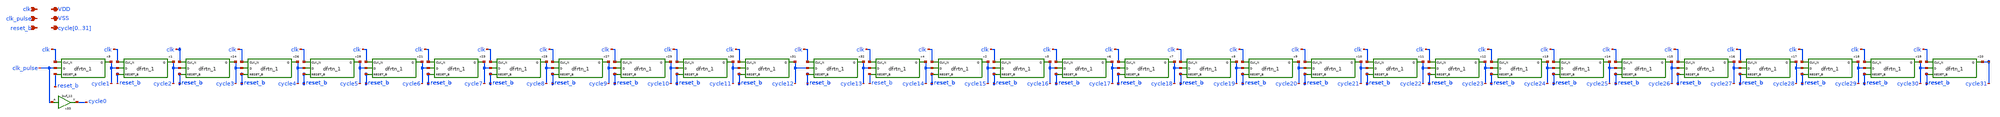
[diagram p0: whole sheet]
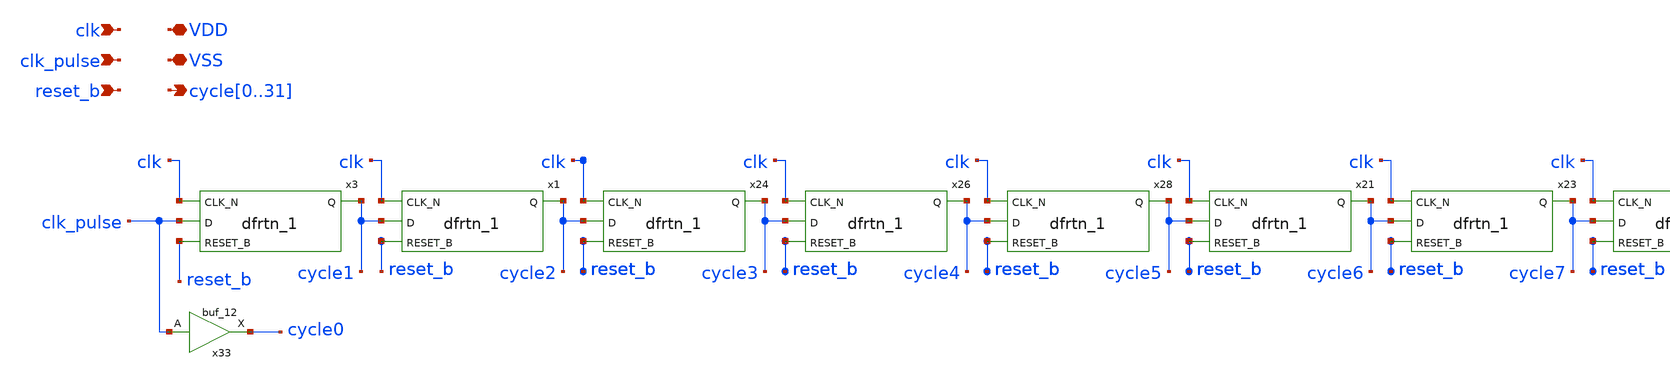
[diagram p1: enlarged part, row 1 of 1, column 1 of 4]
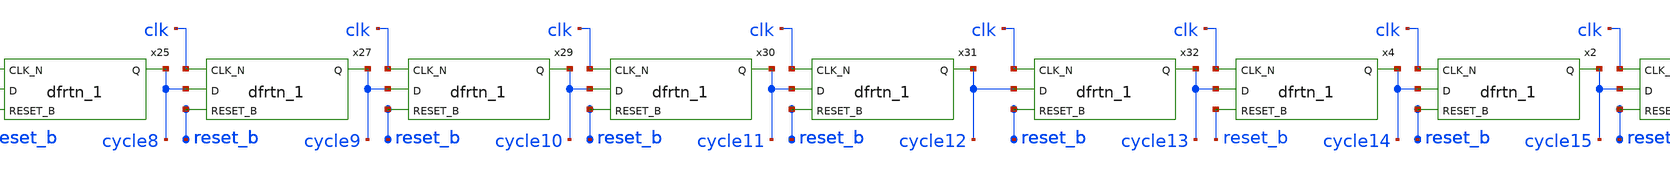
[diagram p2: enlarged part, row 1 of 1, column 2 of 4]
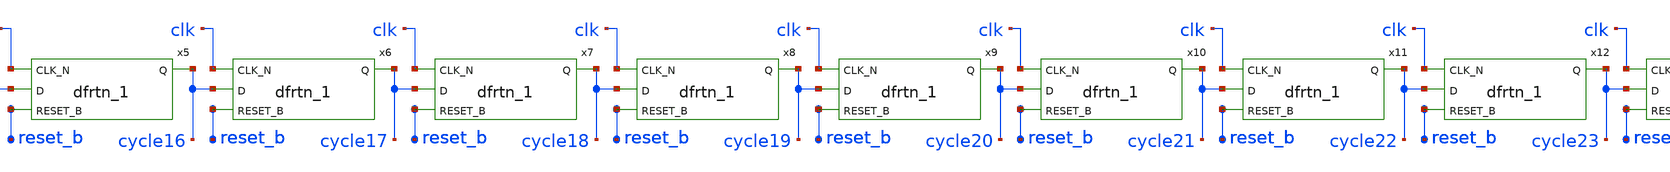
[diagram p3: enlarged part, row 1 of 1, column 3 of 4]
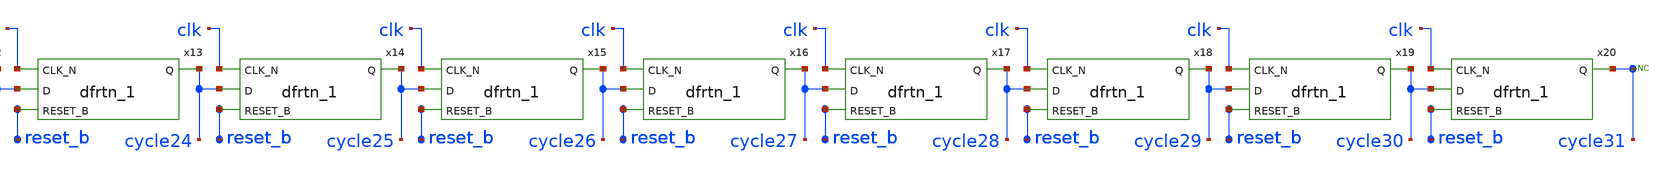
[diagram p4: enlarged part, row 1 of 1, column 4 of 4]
** sch_path: xschem/src/clock_pulse_delay_line/clock_pulse_delay_line.sch
**.subckt clock_pulse_delay_line clk_pulse
*+ cycle0,cycle1,cycle2,cycle3,cycle4,cycle5,cycle6,cycle7,cycle8,cycle9,cycle10,cycle11,cycle12,cycle13,cycle14,cycle15,cycle16,cycle17,cycle18,cycle19,cycle20,cycle21,cycle22,cycle23,cycle24,cycle25,cycle26,cycle27,cycle28,cycle29,cycle30,cycle31 VSS VDD clk reset_b
*.ipin clk_pulse
*.opin
*+ cycle0,cycle1,cycle2,cycle3,cycle4,cycle5,cycle6,cycle7,cycle8,cycle9,cycle10,cycle11,cycle12,cycle13,cycle14,cycle15,cycle16,cycle17,cycle18,cycle19,cycle20,cycle21,cycle22,cycle23,cycle24,cycle25,cycle26,cycle27,cycle28,cycle29,cycle30,cycle31
*.iopin VSS
*.iopin VDD
*.ipin clk
*.ipin reset_b
* noconn cycle31
x3 clk clk_pulse reset_b VSS VSS VDD VDD cycle1 sky130_fd_sc_hd__dfrtn_1
x1 clk cycle1 reset_b VSS VSS VDD VDD cycle2 sky130_fd_sc_hd__dfrtn_1
x24 clk cycle2 reset_b VSS VSS VDD VDD cycle3 sky130_fd_sc_hd__dfrtn_1
x26 clk cycle3 reset_b VSS VSS VDD VDD cycle4 sky130_fd_sc_hd__dfrtn_1
x28 clk cycle4 reset_b VSS VSS VDD VDD cycle5 sky130_fd_sc_hd__dfrtn_1
x21 clk cycle5 reset_b VSS VSS VDD VDD cycle6 sky130_fd_sc_hd__dfrtn_1
x23 clk cycle6 reset_b VSS VSS VDD VDD cycle7 sky130_fd_sc_hd__dfrtn_1
x25 clk cycle7 reset_b VSS VSS VDD VDD cycle8 sky130_fd_sc_hd__dfrtn_1
x27 clk cycle8 reset_b VSS VSS VDD VDD cycle9 sky130_fd_sc_hd__dfrtn_1
x29 clk cycle9 reset_b VSS VSS VDD VDD cycle10 sky130_fd_sc_hd__dfrtn_1
x30 clk cycle10 reset_b VSS VSS VDD VDD cycle11 sky130_fd_sc_hd__dfrtn_1
x31 clk cycle11 reset_b VSS VSS VDD VDD cycle12 sky130_fd_sc_hd__dfrtn_1
x32 clk cycle12 reset_b VSS VSS VDD VDD cycle13 sky130_fd_sc_hd__dfrtn_1
x4 clk cycle13 reset_b VSS VSS VDD VDD cycle14 sky130_fd_sc_hd__dfrtn_1
x5 clk cycle15 reset_b VSS VSS VDD VDD cycle16 sky130_fd_sc_hd__dfrtn_1
x6 clk cycle16 reset_b VSS VSS VDD VDD cycle17 sky130_fd_sc_hd__dfrtn_1
x7 clk cycle17 reset_b VSS VSS VDD VDD cycle18 sky130_fd_sc_hd__dfrtn_1
x8 clk cycle18 reset_b VSS VSS VDD VDD cycle19 sky130_fd_sc_hd__dfrtn_1
x9 clk cycle19 reset_b VSS VSS VDD VDD cycle20 sky130_fd_sc_hd__dfrtn_1
x10 clk cycle20 reset_b VSS VSS VDD VDD cycle21 sky130_fd_sc_hd__dfrtn_1
x11 clk cycle21 reset_b VSS VSS VDD VDD cycle22 sky130_fd_sc_hd__dfrtn_1
x12 clk cycle22 reset_b VSS VSS VDD VDD cycle23 sky130_fd_sc_hd__dfrtn_1
x13 clk cycle23 reset_b VSS VSS VDD VDD cycle24 sky130_fd_sc_hd__dfrtn_1
x14 clk cycle24 reset_b VSS VSS VDD VDD cycle25 sky130_fd_sc_hd__dfrtn_1
x15 clk cycle25 reset_b VSS VSS VDD VDD cycle26 sky130_fd_sc_hd__dfrtn_1
x16 clk cycle26 reset_b VSS VSS VDD VDD cycle27 sky130_fd_sc_hd__dfrtn_1
x17 clk cycle27 reset_b VSS VSS VDD VDD cycle28 sky130_fd_sc_hd__dfrtn_1
x18 clk cycle28 reset_b VSS VSS VDD VDD cycle29 sky130_fd_sc_hd__dfrtn_1
x19 clk cycle29 reset_b VSS VSS VDD VDD cycle30 sky130_fd_sc_hd__dfrtn_1
x20 clk cycle30 reset_b VSS VSS VDD VDD cycle31 sky130_fd_sc_hd__dfrtn_1
x2 clk cycle14 reset_b VSS VSS VDD VDD cycle15 sky130_fd_sc_hd__dfrtn_1
x33 clk_pulse VSS VSS VDD VDD cycle0 sky130_fd_sc_hd__buf_12
**.ends
.end
